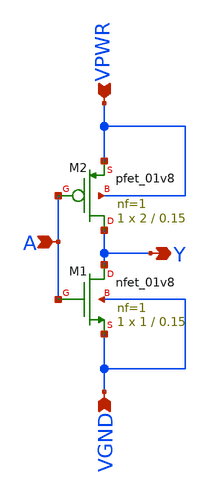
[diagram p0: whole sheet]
** sch_path: inv_vtc.sch
**.subckt inv_vtc A VPWR VGND Y
*.ipin A
*.ipin VPWR
*.ipin VGND
*.opin Y
XM1 Y A VGND VGND sky130_fd_pr__nfet_01v8 L=0.15 W=1 nf=1 ad='int((nf+1)/2) * W/nf * 0.29' as='int((nf+2)/2) * W/nf * 0.29'
+ pd='2*int((nf+1)/2) * (W/nf + 0.29)' ps='2*int((nf+2)/2) * (W/nf + 0.29)' nrd='0.29 / W' nrs='0.29 / W'
+ sa=0 sb=0 sd=0 mult=1 m=1
XM2 Y A VPWR VPWR sky130_fd_pr__pfet_01v8 L=0.15 W=2 nf=1 ad='int((nf+1)/2) * W/nf * 0.29' as='int((nf+2)/2) * W/nf * 0.29'
+ pd='2*int((nf+1)/2) * (W/nf + 0.29)' ps='2*int((nf+2)/2) * (W/nf + 0.29)' nrd='0.29 / W' nrs='0.29 / W'
+ sa=0 sb=0 sd=0 mult=1 m=1
**.ends
.end
